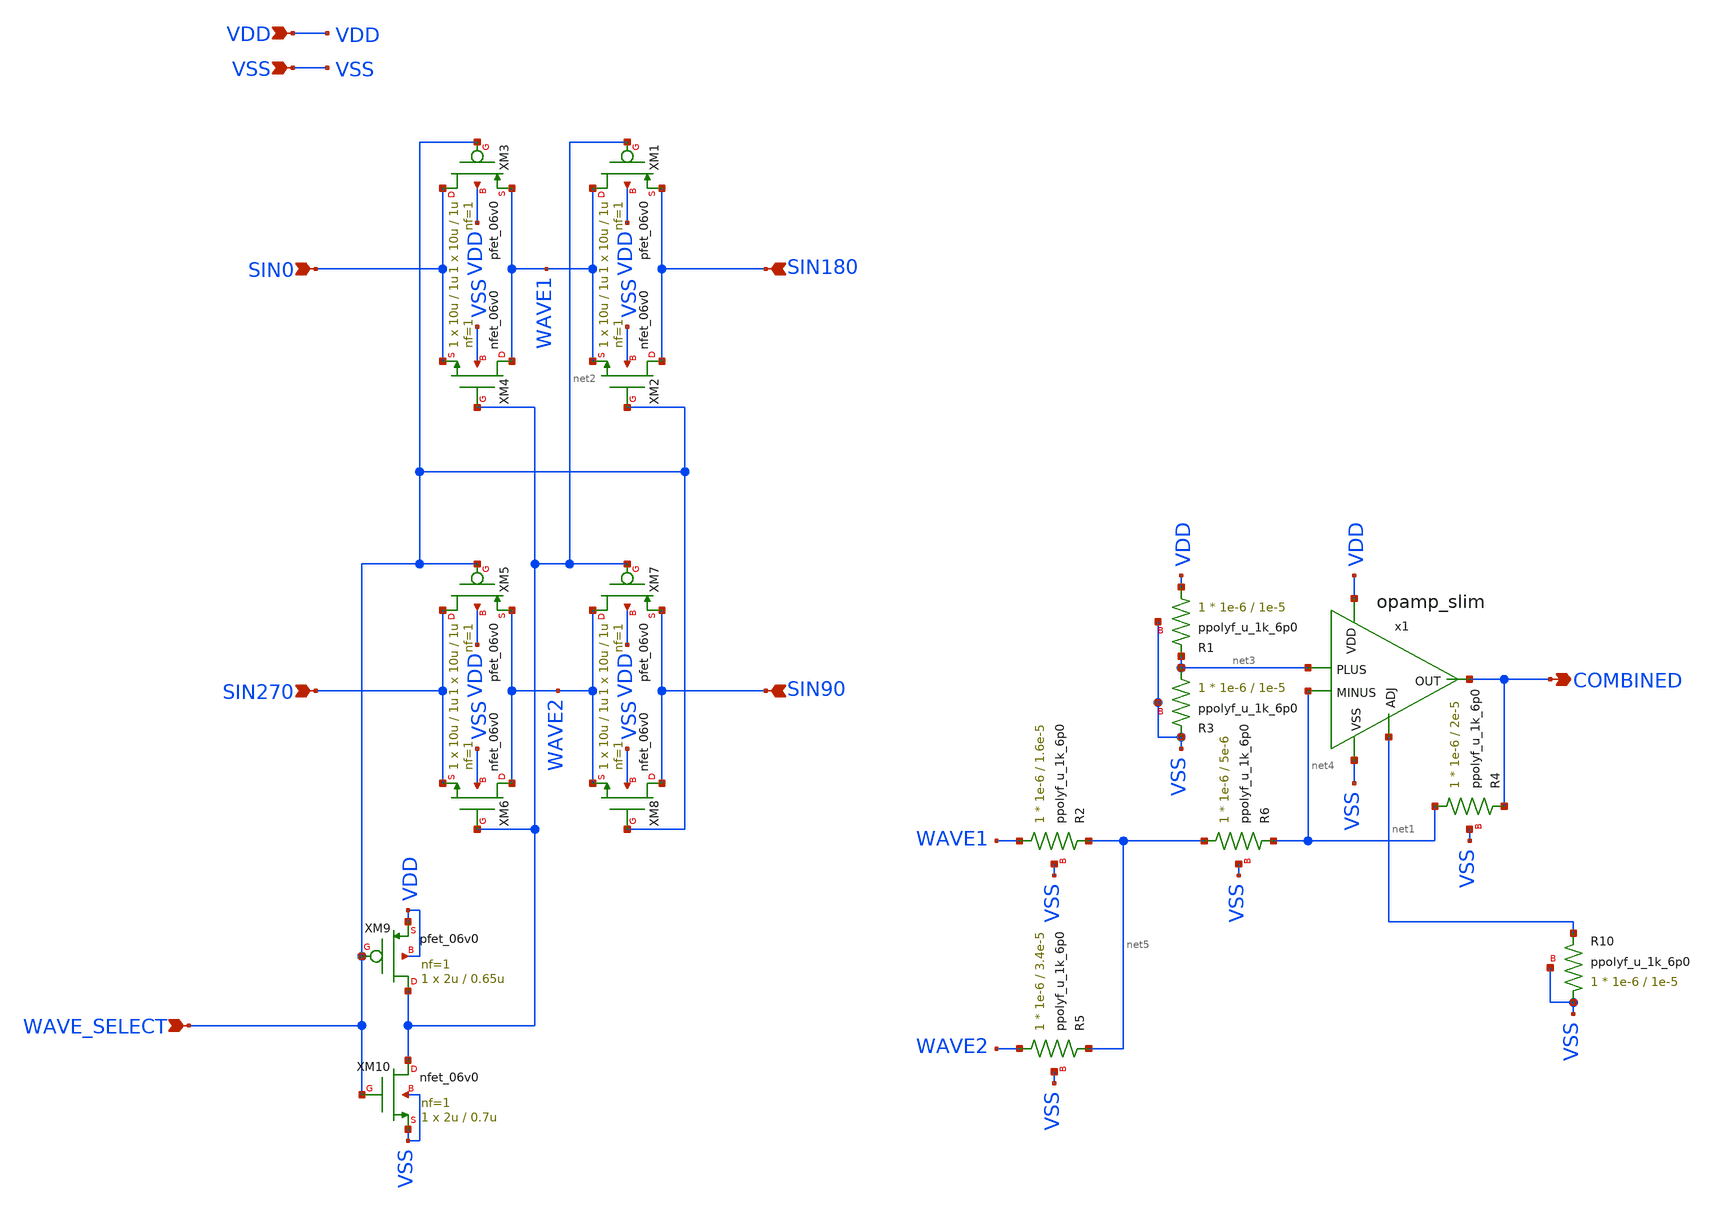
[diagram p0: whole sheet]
** sch_path: macros/Analog/gf180_ntsc/sine_mixer.sch
**.subckt sine_mixer SIN0 SIN90 SIN180 SIN270 WAVE_SELECT COMBINED VDD VSS
*.ipin SIN0
*.ipin SIN90
*.ipin SIN180
*.ipin SIN270
*.ipin WAVE_SELECT
*.opin COMBINED
*.ipin VDD
*.ipin VSS
XR10 VSS net1 VSS ppolyf_u_1k_6p0 r_width=1e-6 r_length=1e-5 m=1
XM3 SIN0 WAVE_SELECT WAVE1 VDD pfet_06v0 L=1u W=10u nf=1 ad='int((nf+1)/2) * W/nf * 0.18u' as='int((nf+2)/2) * W/nf * 0.18u'
+ pd='2*int((nf+1)/2) * (W/nf + 0.18u)' ps='2*int((nf+2)/2) * (W/nf + 0.18u)' nrd='0.18u / W' nrs='0.18u / W'
+ sa=0 sb=0 sd=0 m=1
XM4 WAVE1 net2 SIN0 VSS nfet_06v0 L=1u W=10u nf=1 ad='int((nf+1)/2) * W/nf * 0.18u' as='int((nf+2)/2) * W/nf * 0.18u'
+ pd='2*int((nf+1)/2) * (W/nf + 0.18u)' ps='2*int((nf+2)/2) * (W/nf + 0.18u)' nrd='0.18u / W' nrs='0.18u / W'
+ sa=0 sb=0 sd=0 m=1
XM1 WAVE1 net2 SIN180 VDD pfet_06v0 L=1u W=10u nf=1 ad='int((nf+1)/2) * W/nf * 0.18u' as='int((nf+2)/2) * W/nf * 0.18u'
+ pd='2*int((nf+1)/2) * (W/nf + 0.18u)' ps='2*int((nf+2)/2) * (W/nf + 0.18u)' nrd='0.18u / W' nrs='0.18u / W'
+ sa=0 sb=0 sd=0 m=1
XM2 SIN180 WAVE_SELECT WAVE1 VSS nfet_06v0 L=1u W=10u nf=1 ad='int((nf+1)/2) * W/nf * 0.18u' as='int((nf+2)/2) * W/nf * 0.18u'
+ pd='2*int((nf+1)/2) * (W/nf + 0.18u)' ps='2*int((nf+2)/2) * (W/nf + 0.18u)' nrd='0.18u / W' nrs='0.18u / W'
+ sa=0 sb=0 sd=0 m=1
XM5 SIN270 WAVE_SELECT WAVE2 VDD pfet_06v0 L=1u W=10u nf=1 ad='int((nf+1)/2) * W/nf * 0.18u' as='int((nf+2)/2) * W/nf * 0.18u'
+ pd='2*int((nf+1)/2) * (W/nf + 0.18u)' ps='2*int((nf+2)/2) * (W/nf + 0.18u)' nrd='0.18u / W' nrs='0.18u / W'
+ sa=0 sb=0 sd=0 m=1
XM6 WAVE2 net2 SIN270 VSS nfet_06v0 L=1u W=10u nf=1 ad='int((nf+1)/2) * W/nf * 0.18u' as='int((nf+2)/2) * W/nf * 0.18u'
+ pd='2*int((nf+1)/2) * (W/nf + 0.18u)' ps='2*int((nf+2)/2) * (W/nf + 0.18u)' nrd='0.18u / W' nrs='0.18u / W'
+ sa=0 sb=0 sd=0 m=1
XM7 WAVE2 net2 SIN90 VDD pfet_06v0 L=1u W=10u nf=1 ad='int((nf+1)/2) * W/nf * 0.18u' as='int((nf+2)/2) * W/nf * 0.18u'
+ pd='2*int((nf+1)/2) * (W/nf + 0.18u)' ps='2*int((nf+2)/2) * (W/nf + 0.18u)' nrd='0.18u / W' nrs='0.18u / W'
+ sa=0 sb=0 sd=0 m=1
XM8 SIN90 WAVE_SELECT WAVE2 VSS nfet_06v0 L=1u W=10u nf=1 ad='int((nf+1)/2) * W/nf * 0.18u' as='int((nf+2)/2) * W/nf * 0.18u'
+ pd='2*int((nf+1)/2) * (W/nf + 0.18u)' ps='2*int((nf+2)/2) * (W/nf + 0.18u)' nrd='0.18u / W' nrs='0.18u / W'
+ sa=0 sb=0 sd=0 m=1
XM9 net2 WAVE_SELECT VDD VDD pfet_06v0 L=0.65u W=2u nf=1 ad='int((nf+1)/2) * W/nf * 0.18u' as='int((nf+2)/2) * W/nf * 0.18u'
+ pd='2*int((nf+1)/2) * (W/nf + 0.18u)' ps='2*int((nf+2)/2) * (W/nf + 0.18u)' nrd='0.18u / W' nrs='0.18u / W'
+ sa=0 sb=0 sd=0 m=1
XM10 net2 WAVE_SELECT VSS VSS nfet_06v0 L=0.7u W=2u nf=1 ad='int((nf+1)/2) * W/nf * 0.18u' as='int((nf+2)/2) * W/nf * 0.18u'
+ pd='2*int((nf+1)/2) * (W/nf + 0.18u)' ps='2*int((nf+2)/2) * (W/nf + 0.18u)' nrd='0.18u / W' nrs='0.18u / W'
+ sa=0 sb=0 sd=0 m=1
XR2 WAVE1 net5 VSS ppolyf_u_1k_6p0 r_width=1e-6 r_length=1.6e-5 m=1
x1 VDD COMBINED net3 net4 VSS net1 opamp_slim
XR1 VDD net3 VSS ppolyf_u_1k_6p0 r_width=1e-6 r_length=1e-5 m=1
XR3 net3 VSS VSS ppolyf_u_1k_6p0 r_width=1e-6 r_length=1e-5 m=1
XR4 net4 COMBINED VSS ppolyf_u_1k_6p0 r_width=1e-6 r_length=2e-5 m=1
XR5 WAVE2 net5 VSS ppolyf_u_1k_6p0 r_width=1e-6 r_length=3.4e-5 m=1
XR6 net5 net4 VSS ppolyf_u_1k_6p0 r_width=1e-6 r_length=5e-6 m=1
**.ends

* expanding   symbol:  /foss/designs/Analog/R2R_DAC/xschem/opamp_slim.sym # of pins=6
** sym_path: macros/Analog/R2R_DAC/xschem/opamp_slim.sym
** sch_path: macros/Analog/R2R_DAC/xschem/opamp_slim.sch
.subckt opamp_slim VDD OUT PLUS MINUS VSS ADJ
*.ipin VDD
*.ipin PLUS
*.ipin VSS
*.opin OUT
*.ipin MINUS
*.ipin ADJ
XM2 ADJ ADJ VDD VDD pfet_06v0 L=0.6u W=7u nf=1 ad='int((nf+1)/2) * W/nf * 0.18u' as='int((nf+2)/2) * W/nf * 0.18u'
+ pd='2*int((nf+1)/2) * (W/nf + 0.18u)' ps='2*int((nf+2)/2) * (W/nf + 0.18u)' nrd='0.18u / W' nrs='0.18u / W'
+ sa=0 sb=0 sd=0 m=1
XM9 net1 ADJ VDD VDD pfet_06v0 L=0.6u W=7u nf=1 ad='int((nf+1)/2) * W/nf * 0.18u' as='int((nf+2)/2) * W/nf * 0.18u'
+ pd='2*int((nf+1)/2) * (W/nf + 0.18u)' ps='2*int((nf+2)/2) * (W/nf + 0.18u)' nrd='0.18u / W' nrs='0.18u / W'
+ sa=0 sb=0 sd=0 m=1
XM10 OUT ADJ VDD VDD pfet_06v0 L=0.6u W=25u nf=1 ad='int((nf+1)/2) * W/nf * 0.18u' as='int((nf+2)/2) * W/nf * 0.18u'
+ pd='2*int((nf+1)/2) * (W/nf + 0.18u)' ps='2*int((nf+2)/2) * (W/nf + 0.18u)' nrd='0.18u / W' nrs='0.18u / W'
+ sa=0 sb=0 sd=0 m=1
XM11 net3 MINUS net1 VDD pfet_06v0 L=0.6u W=7u nf=1 ad='int((nf+1)/2) * W/nf * 0.18u' as='int((nf+2)/2) * W/nf * 0.18u'
+ pd='2*int((nf+1)/2) * (W/nf + 0.18u)' ps='2*int((nf+2)/2) * (W/nf + 0.18u)' nrd='0.18u / W' nrs='0.18u / W'
+ sa=0 sb=0 sd=0 m=1
XM12 net2 PLUS net1 VDD pfet_06v0 L=0.6u W=7u nf=1 ad='int((nf+1)/2) * W/nf * 0.18u' as='int((nf+2)/2) * W/nf * 0.18u'
+ pd='2*int((nf+1)/2) * (W/nf + 0.18u)' ps='2*int((nf+2)/2) * (W/nf + 0.18u)' nrd='0.18u / W' nrs='0.18u / W'
+ sa=0 sb=0 sd=0 m=1
XM13 net3 net3 VSS VSS nfet_06v0 L=0.6u W=5u nf=1 ad='int((nf+1)/2) * W/nf * 0.18u' as='int((nf+2)/2) * W/nf * 0.18u'
+ pd='2*int((nf+1)/2) * (W/nf + 0.18u)' ps='2*int((nf+2)/2) * (W/nf + 0.18u)' nrd='0.18u / W' nrs='0.18u / W'
+ sa=0 sb=0 sd=0 m=1
XM14 net2 net3 VSS VSS nfet_06v0 L=0.6u W=5u nf=1 ad='int((nf+1)/2) * W/nf * 0.18u' as='int((nf+2)/2) * W/nf * 0.18u'
+ pd='2*int((nf+1)/2) * (W/nf + 0.18u)' ps='2*int((nf+2)/2) * (W/nf + 0.18u)' nrd='0.18u / W' nrs='0.18u / W'
+ sa=0 sb=0 sd=0 m=1
XM15 OUT net2 VSS VSS nfet_06v0 L=0.6u W=20u nf=1 ad='int((nf+1)/2) * W/nf * 0.18u' as='int((nf+2)/2) * W/nf * 0.18u'
+ pd='2*int((nf+1)/2) * (W/nf + 0.18u)' ps='2*int((nf+2)/2) * (W/nf + 0.18u)' nrd='0.18u / W' nrs='0.18u / W'
+ sa=0 sb=0 sd=0 m=1
.ends

.end
